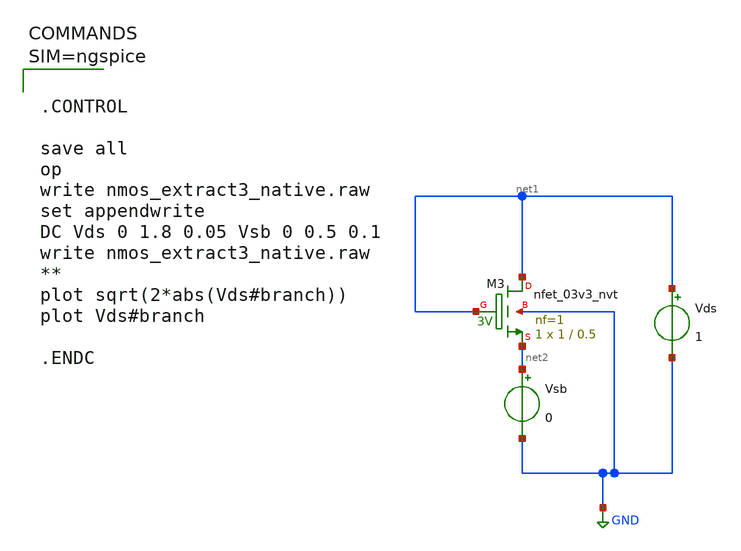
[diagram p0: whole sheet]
** sch_path: work/xschem/nmos_extract3_native.sch
**.subckt nmos_extract3_native
Vds net1 GND 1
Vsb net2 GND 0
XM3 net1 net1 net2 GND sky130_fd_pr__nfet_03v3_nvt L=0.5 W=1 nf=1 ad='int((1 + 1)/2) * 1 / 1 * 0.29'
+ as='int((1 + 2)/2) * 1 / 1 * 0.29' pd='2*int((1 + 1)/2) * (1 / 1 + 0.29)' ps='2*int((1 + 2)/2) * (1 / 1 + 0.29)'
+ nrd='0.29 / 1 ' nrs='0.29 / 1 ' sa=0 sb=0 sd=0 mult=1 m=1
**** begin user architecture code



.CONTROL

save all
op
write nmos_extract3_native.raw
set appendwrite
DC Vds 0 1.8 0.05 Vsb 0 0.5 0.1
write nmos_extract3_native.raw
**
plot sqrt(2*abs(Vds#branch))
plot Vds#branch

.ENDC




** opencircuitdesign pdks install
.lib $::SKYWATER_MODELS/sky130.lib.spice tt

**** end user architecture code
**.ends
.GLOBAL GND
.end
